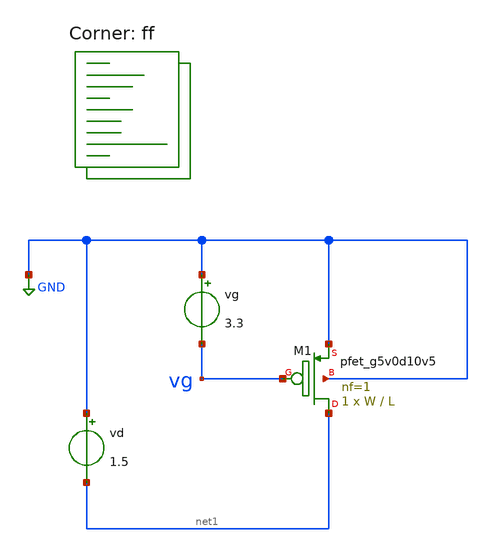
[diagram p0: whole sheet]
** sch_path: charac/pfet.sch
**.subckt pfet
vd GND net1 1.5
vg GND vg 3.3
XM1 net1 vg GND GND sky130_fd_pr__pfet_g5v0d10v5 L=L W=W nf=1 ad='int((nf+1)/2) * W/nf * 0.29' as='int((nf+2)/2) * W/nf * 0.29'
+ pd='2*int((nf+1)/2) * (W/nf + 0.29)' ps='2*int((nf+2)/2) * (W/nf + 0.29)' nrd='0.29 / W' nrs='0.29 / W'
+ sa=0 sb=0 sd=0 mult=1 m=1
**** begin user architecture code
.lib $::SKYWATER_MODELS/sky130.lib.spice ff

* ngspice commands
.param W=5
.param L=0.5
.options savecurrents
.dc vg 100m 3.3 10m
.control
  set device = 'pfet'
  set corner = 'ff'
* === short channel
  set lengths = '0.5 0.6 0.8 1 1.5'
  set channel = 'sc'
* name files
  set vgs_file = {$device}_vgs_{$channel}_{$corner}.ps
  set gm_file = {$device}_gm_{$channel}_{$corner}.ps
  set gds_file = {$device}_gds_{$channel}_{$corner}.ps
  set gain_file = {$device}_gain_{$channel}_{$corner}.ps
* initialize plots
  set plot_vgs = ' '
  set plot_gm = ' '
  set plot_gds = ' '
  set plot_gain = ' '
  set plot_title = '{$device} CORNER = {$corner} L = {$lengths}'
* loop through channel lengths and run DC analysis
  foreach l_act 0.5 0.6 0.8 1 1.5
    alterparam L = $l_act
    reset
    save all
    save @m.xm1.msky130_fd_pr__pfet_g5v0d10v5[gm]
    save @m.xm1.msky130_fd_pr__pfet_g5v0d10v5[gds]
    save @m.xm1.msky130_fd_pr__pfet_g5v0d10v5[id]
    save @m.xm1.msky130_fd_pr__pfet_g5v0d10v5[w]
    save @m.xm1.msky130_fd_pr__pfet_g5v0d10v5[l]
    echo l = $l_act
    run
    remzerovec
* compute parameters
    let idn = @m.xm1.msky130_fd_pr__pfet_g5v0d10v5[id] / ( @m.xm1.msky130_fd_pr__pfet_g5v0d10v5[w] /
+ @m.xm1.msky130_fd_pr__pfet_g5v0d10v5[l] )
    let gm = @m.xm1.msky130_fd_pr__pfet_g5v0d10v5[gm] / @m.xm1.msky130_fd_pr__pfet_g5v0d10v5[id]
    let gds = @m.xm1.msky130_fd_pr__pfet_g5v0d10v5[gds] / @m.xm1.msky130_fd_pr__pfet_g5v0d10v5[id]
    let gain = @m.xm1.msky130_fd_pr__pfet_g5v0d10v5[gm] / @m.xm1.msky130_fd_pr__pfet_g5v0d10v5[gds]
* update plots
    set plot_vgs = ( $plot_vgs vg vs {$curplot}.idn )
    set plot_gm = ( $plot_gm {$curplot}.gm vs {$curplot}.idn )
    set plot_gds = ( $plot_gds {$curplot}.gds vs {$curplot}.idn )
    set plot_gain = ( $plot_gain {$curplot}.gain vs {$curplot}.idn )
  end
* export graphics
  set nolegend
  hardcopy $vgs_file $plot_vgs xlog xlimit 1e-12 1e-3 xlabel 'id*' ylabel 'vgs' title $plot_title
  hardcopy $gm_file $plot_gm xlog xlimit 1e-12 1e-3 xlabel 'id*' ylabel 'gm / Id' title $plot_title
  hardcopy $gds_file $plot_gds loglog xlimit 1e-12 1e-3 xlabel 'id*' ylabel 'gds / Id' title $plot_title
  hardcopy $gain_file $plot_gain loglog xlimit 1e-12 1e-3 xlabel 'id*' ylabel 'gain' title $plot_title

* === long channel
  set lengths = '2 3 4 5 6 7 8'
  set channel = 'lc'
* name files
  set vgs_file = {$device}_vgs_{$channel}_{$corner}.ps
  set gm_file = {$device}_gm_{$channel}_{$corner}.ps
  set gds_file = {$device}_gds_{$channel}_{$corner}.ps
  set gain_file = {$device}_gain_{$channel}_{$corner}.ps
* initialize plots
  set plot_vgs = ' '
  set plot_gm = ' '
  set plot_gds = ' '
  set plot_gain = ' '
  set plot_title = '{$device} CORNER = {$corner} L = {$lengths}'
* loop through channel lengths and run DC analysis
  foreach l_act 2 3 4 5 6 7 8
    alterparam L = $l_act
    reset
    save all
    save @m.xm1.msky130_fd_pr__pfet_g5v0d10v5[gm]
    save @m.xm1.msky130_fd_pr__pfet_g5v0d10v5[gds]
    save @m.xm1.msky130_fd_pr__pfet_g5v0d10v5[id]
    save @m.xm1.msky130_fd_pr__pfet_g5v0d10v5[w]
    save @m.xm1.msky130_fd_pr__pfet_g5v0d10v5[l]
    echo l = $l_act
    run
    remzerovec
* compute parameters
    let idn = @m.xm1.msky130_fd_pr__pfet_g5v0d10v5[id] / ( @m.xm1.msky130_fd_pr__pfet_g5v0d10v5[w] /
+ @m.xm1.msky130_fd_pr__pfet_g5v0d10v5[l] )
    let gm = @m.xm1.msky130_fd_pr__pfet_g5v0d10v5[gm] / @m.xm1.msky130_fd_pr__pfet_g5v0d10v5[id]
    let gds = @m.xm1.msky130_fd_pr__pfet_g5v0d10v5[gds] / @m.xm1.msky130_fd_pr__pfet_g5v0d10v5[id]
    let gain = @m.xm1.msky130_fd_pr__pfet_g5v0d10v5[gm] / @m.xm1.msky130_fd_pr__pfet_g5v0d10v5[gds]
* update plots
    set plot_vgs = ( $plot_vgs vg vs {$curplot}.idn )
    set plot_gm = ( $plot_gm {$curplot}.gm vs {$curplot}.idn )
    set plot_gds = ( $plot_gds {$curplot}.gds vs {$curplot}.idn )
    set plot_gain = ( $plot_gain {$curplot}.gain vs {$curplot}.idn )
  end
* export graphics
  set nolegend
  hardcopy $vgs_file $plot_vgs xlog xlimit 1e-12 1e-3 xlabel 'id*' ylabel 'vgs' title $plot_title
  hardcopy $gm_file $plot_gm xlog xlimit 1e-12 1e-3 xlabel 'id*' ylabel 'gm / Id' title $plot_title
  hardcopy $gds_file $plot_gds loglog xlimit 1e-12 1e-3 xlabel 'id*' ylabel 'gds / Id' title $plot_title
  hardcopy $gain_file $plot_gain loglog xlimit 1e-12 1e-3 xlabel 'id*' ylabel 'gain' title $plot_title
  quit
.endc


**** end user architecture code
**.ends
.GLOBAL GND
.end
